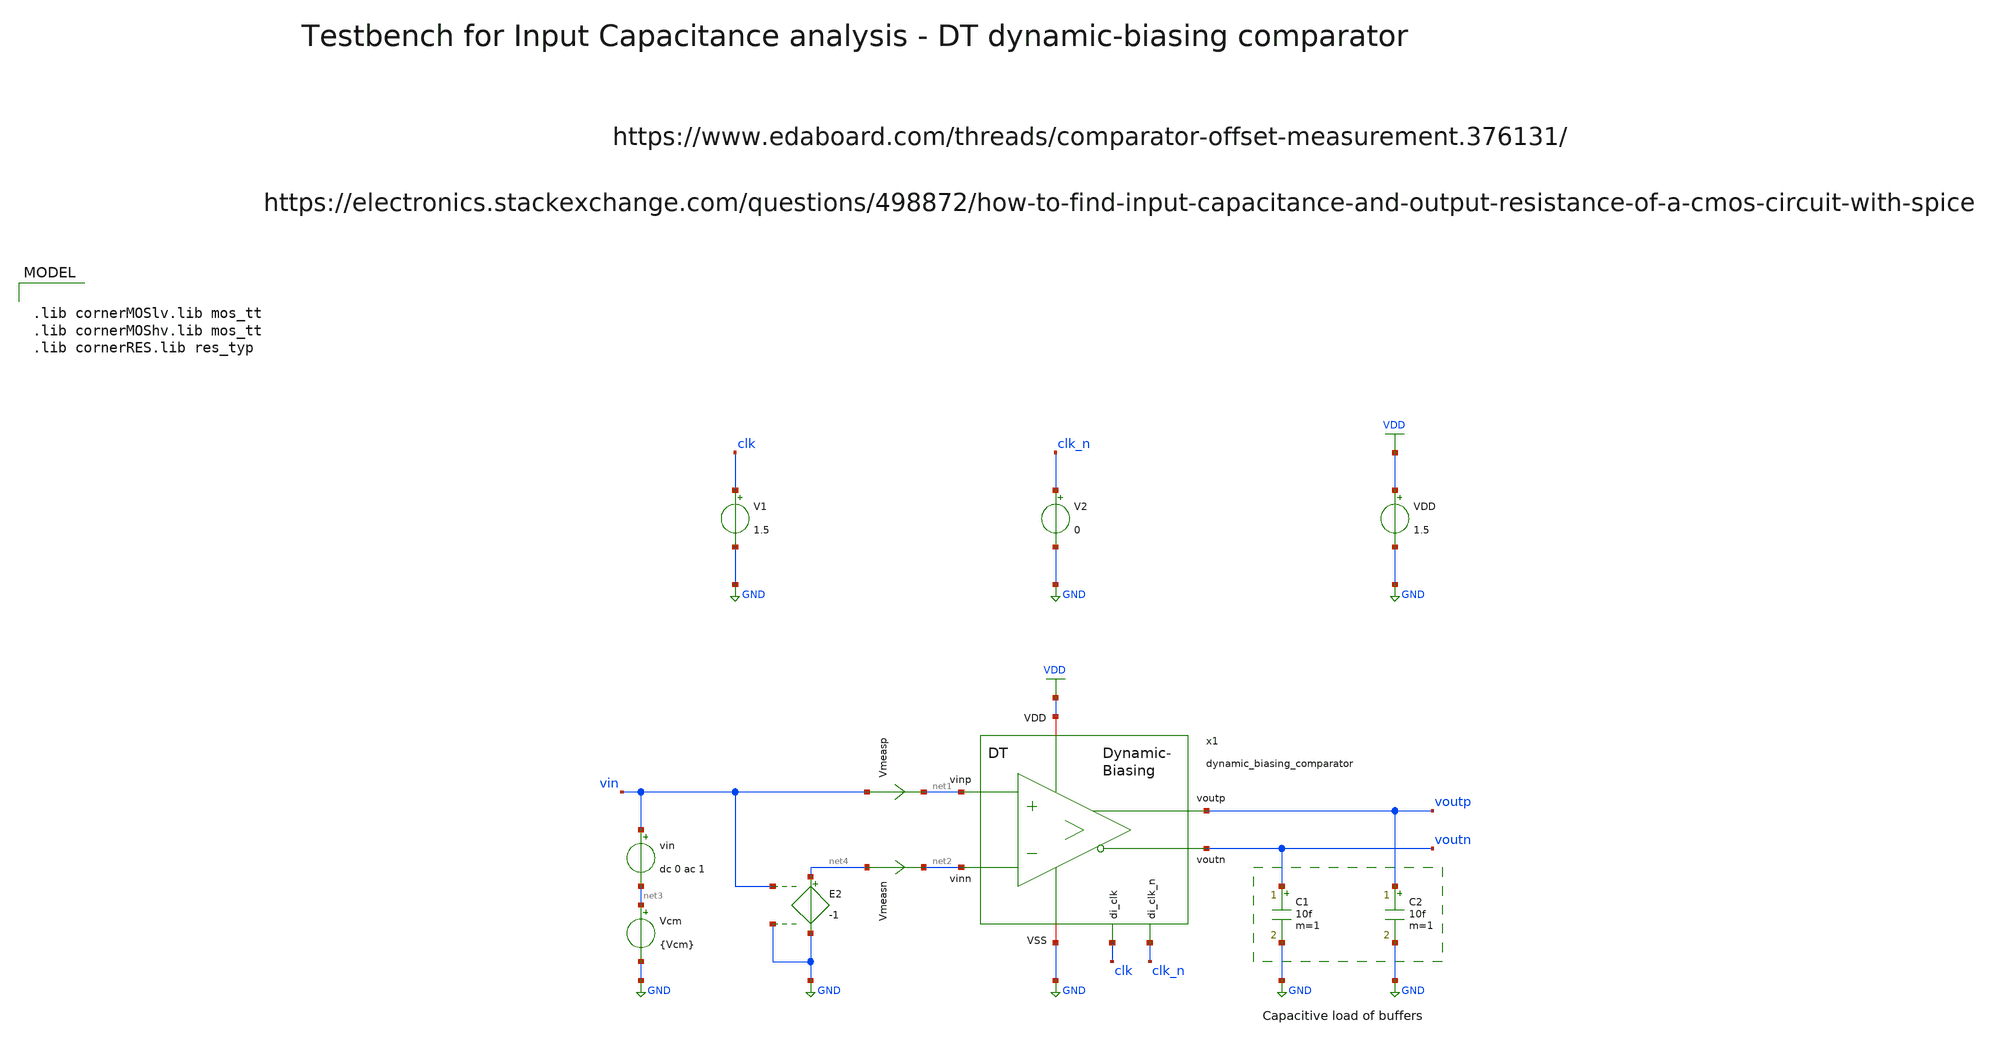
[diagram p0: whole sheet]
** sch_path: SG13G2_ATBS-ADC-main/xschem/comparator/discrete_time/Dynamic-biasing/testbenches/dynamic_biasing_comparator_tb_ac_cin.sch
**.subckt dynamic_biasing_comparator_tb_ac_cin
VDD VDD GND 1.5
V1 clk GND 1.5
V2 clk_n GND 0
C1 voutn GND 10f m=1
C2 voutp GND 10f m=1
Vmeasp vin net1 0
.save i(vmeasp)
Vmeasn net4 net2 0
.save i(vmeasn)
vin vin net3 dc 0 ac 1
Vcm net3 GND {Vcm}
E2 net4 GND vin GND -1
x1 clk_n clk VDD voutp net1 GND voutn net2 dynamic_biasing_comparator
**** begin user architecture code

.lib cornerMOSlv.lib mos_tt
.lib cornerMOShv.lib mos_tt
.lib cornerRES.lib res_typ



.param temp=27
.param Vcm=0.75
.options savecurrents reltol=1e-3 abstol=1e-12 gmin=1e-15
.control
save all

* User Constants
let fstart = 1
let fstop = 1G

* Operating Point Analysis
op
remzerovec
write dynamic_biasing_comparator_tb_ac_cin.raw
set appendwrite

* AC Analysis
ac dec 101 $&fstart $&fstop
remzerovec
write dynamic_biasing_comparator_tb_ac_cin.raw

* Plotting Cinp
let Cinp = mag(i(Vmeasp)) / (2 * 3.14 * frequency)
plot Cinp

* Plotting Cinn
let Cinn = mag(i(Vmeasn)) / (2 * 3.14 * frequency)
plot Cinn

* Measure avg. Cinp & Cinn
meas ac Cinp_avg AVG Cinp from=fstart to=fstop
meas ac Cinn_avg AVG Cinn from=fstart to=fstop

* Writing Data
set wr_singlescale
set wr_vecnames
wrdata
+ /foss/designs/SG13G2_ATBS-ADC-main/python/plot_simulations/data/dynamic_biasing_comparator_tb_ac_cin.txt v(Cinp) v(Cinn)

*quit
.endc

**** end user architecture code
**.ends

* expanding   symbol:  comparator/discrete_time/Dynamic-biasing/dynamic_biasing_comparator.sym # of
*+ pins=8
** sym_path: SG13G2_ATBS-ADC-main/xschem/comparator/discrete_time/Dynamic-biasing/dynamic_biasing_comparator.sym
** sch_path: SG13G2_ATBS-ADC-main/xschem/comparator/discrete_time/Dynamic-biasing/dynamic_biasing_comparator.sch
.subckt dynamic_biasing_comparator di_clk_n di_clk VDD voutp vinp VSS voutn vinn
*.iopin VDD
*.opin voutp
*.opin voutn
*.ipin di_clk_n
*.iopin VSS
*.ipin vinp
*.ipin vinn
*.ipin di_clk
XM3a vs di_clk vctail VSS sg13_lv_nmos w=1.0u l=0.13u ng=1 m=1 mm_ok=1
XM12 voutp di_clk_n VSS VSS sg13_lv_nmos w=1.0u l=0.13u ng=1 m=1 mm_ok=1
XM8 net1 voutn VDD VDD sg13_lv_pmos w=2.0u l=0.13u ng=2 m=1 mm_ok=1
XM10 voutp voutn VSS VSS sg13_lv_nmos w=1.0u l=0.13u ng=1 m=1 mm_ok=1
XM11 voutn voutp VSS VSS sg13_lv_nmos w=1.0u l=0.13u ng=1 m=1 mm_ok=1
XM13 voutn di_clk_n VSS VSS sg13_lv_nmos w=1.0u l=0.13u ng=1 m=1 mm_ok=1
CPn vcpn VSS 300f m=1
CPp vcpp VSS 300f m=1
XM9 net2 voutp VDD VDD sg13_lv_pmos w=2.0u l=0.13u ng=2 m=1 mm_ok=1
XM6 voutp vcpn net1 VDD sg13_lv_pmos w=2.0u l=0.13u ng=2 m=1 mm_ok=1
XM7 voutn vcpp net2 VDD sg13_lv_pmos w=2.0u l=0.13u ng=2 m=1 mm_ok=1
CTAIL vctail VSS 600f m=1
XM3b vctail di_clk_n VSS VSS sg13_lv_nmos w=1.0u l=0.13u ng=1 m=1 mm_ok=1
XM1 vcpn vinp vs VSS sg13_lv_nmos w=1.0u l=0.13u ng=1 m=1 mm_ok=1
XM2 vcpp vinn vs VSS sg13_lv_nmos w=1.0u l=0.13u ng=1 m=1 mm_ok=1
XM4 vcpn di_clk VDD VDD sg13_lv_pmos w=1.0u l=0.13u ng=1 m=1 mm_ok=1
XM5 vcpp di_clk VDD VDD sg13_lv_pmos w=1.0u l=0.13u ng=1 m=1 mm_ok=1
.ends

.GLOBAL GND
.GLOBAL VDD
.end
